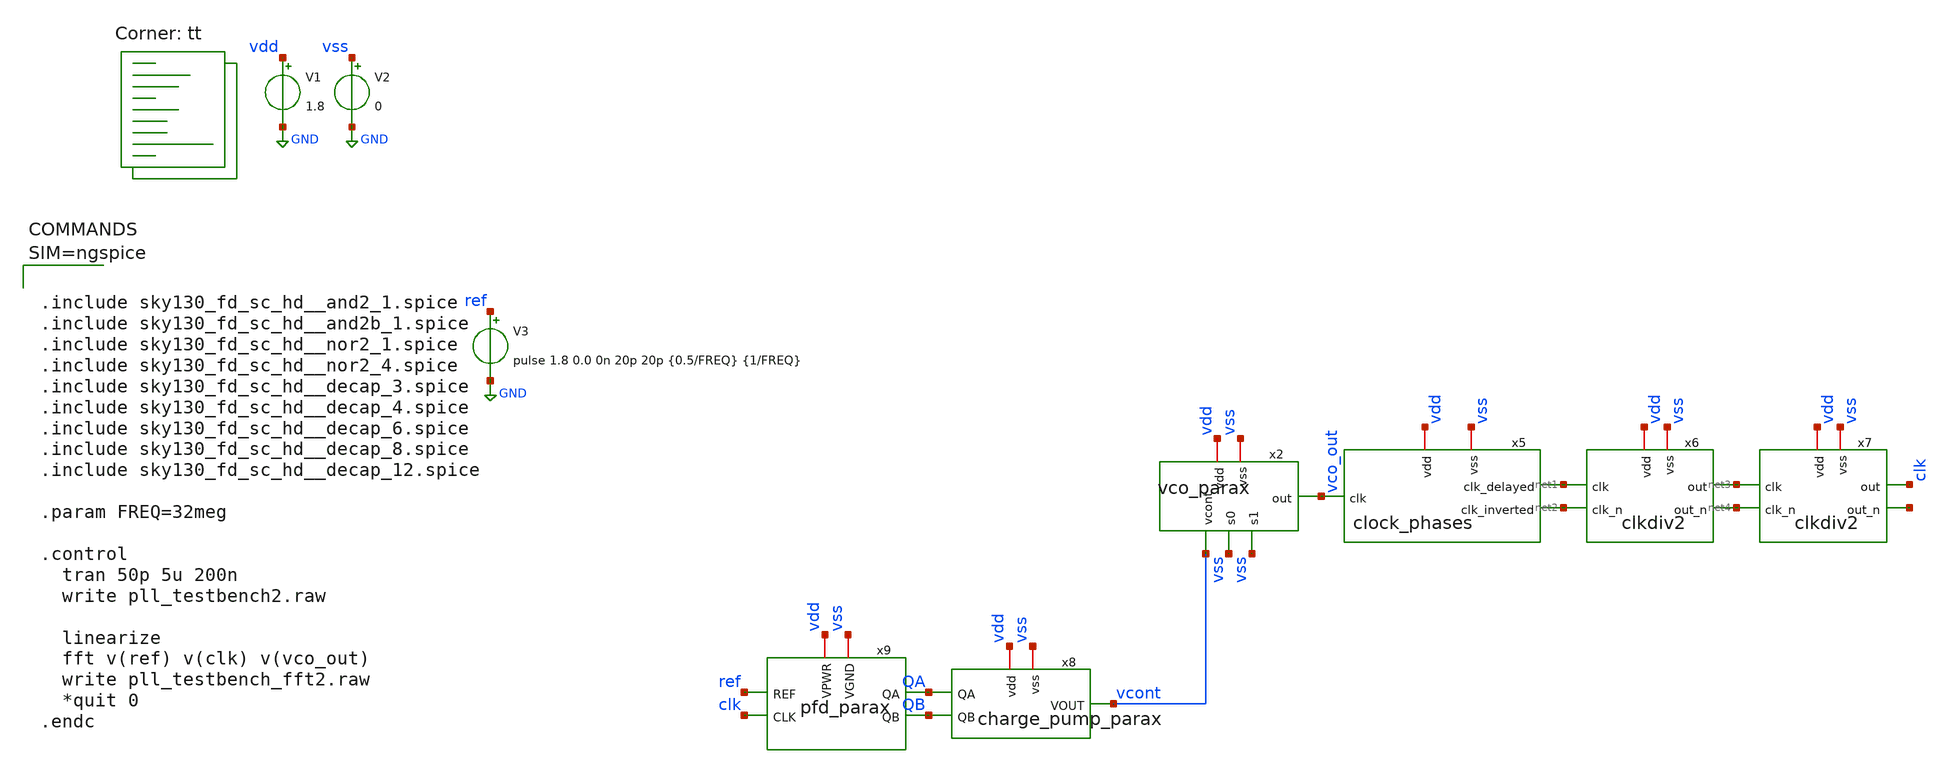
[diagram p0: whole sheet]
** sch_path: xschem/pll_testbench2.sch
**.subckt pll_testbench2
V1 vdd GND 1.8
V2 vss GND 0
x2 vdd vcont vss vss vco_out vss vco_parax
V3 ref GND pulse 1.8 0.0 0n 20p 20p {0.5/FREQ} {1/FREQ}
x5 vdd net1 vco_out net2 vss clock_phases
x6 vdd vss net3 net4 net2 net1 clkdiv2
x7 vdd vss clk net5 net4 net3 clkdiv2
x8 vdd vss QA QB vcont charge_pump_parax
x9 vdd vss ref QA QB clk pfd_parax
**** begin user architecture code
.lib $::SKYWATER_MODELS/sky130.lib.spice tt



.include sky130_fd_sc_hd__and2_1.spice
.include sky130_fd_sc_hd__and2b_1.spice
.include sky130_fd_sc_hd__nor2_1.spice
.include sky130_fd_sc_hd__nor2_4.spice
.include sky130_fd_sc_hd__decap_3.spice
.include sky130_fd_sc_hd__decap_4.spice
.include sky130_fd_sc_hd__decap_6.spice
.include sky130_fd_sc_hd__decap_8.spice
.include sky130_fd_sc_hd__decap_12.spice

.param FREQ=32meg

.control
  tran 50p 5u 200n
  write pll_testbench2.raw

  linearize
  fft v(ref) v(clk) v(vco_out)
  write pll_testbench_fft2.raw
  *quit 0
.endc



**** end user architecture code
**.ends

* expanding   symbol:  vco_parax.sym # of pins=6
** sym_path: xschem/vco.sym
.include [file normalize ../mag/vco.sim.spice]

* expanding   symbol:  clock_phases.sym # of pins=5
** sym_path: xschem/clock_phases.sym
** sch_path: xschem/clock_phases.sch
.subckt clock_phases vdd clk_delayed clk clk_inverted vss
*.ipin clk
*.iopin vdd
*.opin clk_delayed
*.opin clk_inverted
*.iopin vss
XM3 net2 clk vss GND sky130_fd_pr__nfet_01v8 L=0.15 W=1 nf=1 ad='int((nf+1)/2) * W/nf * 0.29' as='int((nf+2)/2) * W/nf * 0.29'
+ pd='2*int((nf+1)/2) * (W/nf + 0.29)' ps='2*int((nf+2)/2) * (W/nf + 0.29)' nrd='0.29 / W' nrs='0.29 / W'
+ sa=0 sb=0 sd=0 mult=1 m=1
XM4 net2 clk vdd VDD sky130_fd_pr__pfet_01v8 L=0.15 W=1 nf=2 ad='int((nf+1)/2) * W/nf * 0.29' as='int((nf+2)/2) * W/nf * 0.29'
+ pd='2*int((nf+1)/2) * (W/nf + 0.29)' ps='2*int((nf+2)/2) * (W/nf + 0.29)' nrd='0.29 / W' nrs='0.29 / W'
+ sa=0 sb=0 sd=0 mult=1 m=1
XM5 net1 vdd clk GND sky130_fd_pr__nfet_01v8 L=0.15 W=1 nf=1 ad='int((nf+1)/2) * W/nf * 0.29' as='int((nf+2)/2) * W/nf * 0.29'
+ pd='2*int((nf+1)/2) * (W/nf + 0.29)' ps='2*int((nf+2)/2) * (W/nf + 0.29)' nrd='0.29 / W' nrs='0.29 / W'
+ sa=0 sb=0 sd=0 mult=1 m=1
XM6 net1 vss clk VDD sky130_fd_pr__pfet_01v8 L=0.15 W=1 nf=2 ad='int((nf+1)/2) * W/nf * 0.29' as='int((nf+2)/2) * W/nf * 0.29'
+ pd='2*int((nf+1)/2) * (W/nf + 0.29)' ps='2*int((nf+2)/2) * (W/nf + 0.29)' nrd='0.29 / W' nrs='0.29 / W'
+ sa=0 sb=0 sd=0 mult=1 m=1
XM7 clk_delayed net2 vss GND sky130_fd_pr__nfet_01v8 L=0.15 W=1 nf=1 ad='int((nf+1)/2) * W/nf * 0.29'
+ as='int((nf+2)/2) * W/nf * 0.29' pd='2*int((nf+1)/2) * (W/nf + 0.29)' ps='2*int((nf+2)/2) * (W/nf + 0.29)'
+ nrd='0.29 / W' nrs='0.29 / W' sa=0 sb=0 sd=0 mult=1 m=1
XM8 clk_delayed net2 vdd VDD sky130_fd_pr__pfet_01v8 L=0.15 W=1 nf=2 ad='int((nf+1)/2) * W/nf * 0.29'
+ as='int((nf+2)/2) * W/nf * 0.29' pd='2*int((nf+1)/2) * (W/nf + 0.29)' ps='2*int((nf+2)/2) * (W/nf + 0.29)'
+ nrd='0.29 / W' nrs='0.29 / W' sa=0 sb=0 sd=0 mult=1 m=1
XM9 clk_inverted net1 vss GND sky130_fd_pr__nfet_01v8 L=0.15 W=1 nf=1 ad='int((nf+1)/2) * W/nf * 0.29'
+ as='int((nf+2)/2) * W/nf * 0.29' pd='2*int((nf+1)/2) * (W/nf + 0.29)' ps='2*int((nf+2)/2) * (W/nf + 0.29)'
+ nrd='0.29 / W' nrs='0.29 / W' sa=0 sb=0 sd=0 mult=1 m=1
XM10 clk_inverted net1 vdd VDD sky130_fd_pr__pfet_01v8 L=0.15 W=1 nf=2 ad='int((nf+1)/2) * W/nf * 0.29'
+ as='int((nf+2)/2) * W/nf * 0.29' pd='2*int((nf+1)/2) * (W/nf + 0.29)' ps='2*int((nf+2)/2) * (W/nf + 0.29)'
+ nrd='0.29 / W' nrs='0.29 / W' sa=0 sb=0 sd=0 mult=1 m=1
.ends


* expanding   symbol:  clkdiv2.sym # of pins=6
** sym_path: xschem/clkdiv2.sym
** sch_path: xschem/clkdiv2.sch
.subckt clkdiv2 vdd vss out out_n clk_n clk
*.iopin vdd
*.opin out
*.iopin vss
*.ipin clk
*.opin out_n
*.ipin clk_n
x2 vdd vss net1 net2 out_n out clk latch_parax
x3 vdd vss out_n out net2 net1 clk_n latch_parax
.ends


* expanding   symbol:  charge_pump_parax.sym # of pins=5
** sym_path: xschem/charge_pump.sym
.include [file normalize ../mag/charge_pump.sim.spice]

* expanding   symbol:  pfd_parax.sym # of pins=6
** sym_path: xschem/pfd.sym
.include [file normalize ../mag/pfd.sim.spice]

* expanding   symbol:  latch_parax.sym # of pins=7
** sym_path: xschem/latch.sym
.include [file normalize ../mag/latch.sim.spice]
.GLOBAL GND
.end
